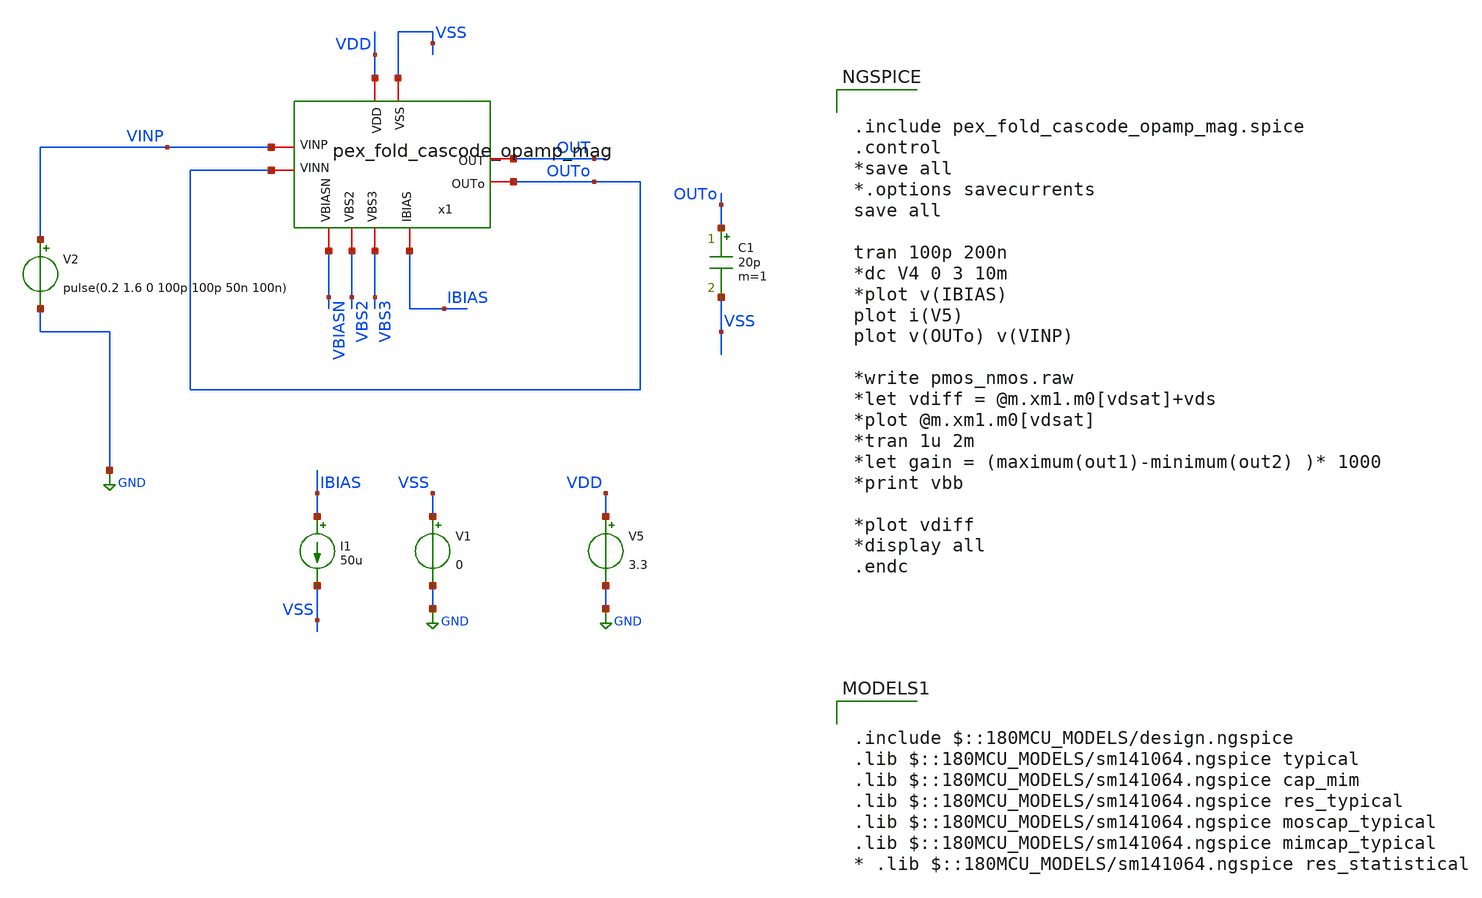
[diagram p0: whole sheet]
** sch_path: SCOP_INPUT_AND_MUX_PAKISTAN_03/Xschem/Folded_single/folded_single_TB_slew.sch
**.subckt folded_single_TB_slew
V5 VDD GND 3.3
V2 VINP GND pulse(0.2 1.6 0 100p 100p 50n 100n)
V1 VSS GND 0
I1 IBIAS VSS 50u
C1 OUTo VSS 20p m=1
x1 OUT VDD VSS OUTo VINP IBIAS VBS2 VBS3 VBIASN OUTo pex_fold_cascode_opamp_mag
**** begin user architecture code


.include pex_fold_cascode_opamp_mag.spice
.control
*save all
*.options savecurrents
save all

tran 100p 200n
*dc V4 0 3 10m
*plot v(IBIAS)
plot i(V5)
plot v(OUTo) v(VINP)

*write pmos_nmos.raw
*let vdiff = @m.xm1.m0[vdsat]+vds
*plot @m.xm1.m0[vdsat]
*tran 1u 2m
*let gain = (maximum(out1)-minimum(out2) )* 1000
*print vbb

*plot vdiff
*display all
.endc



.include $::180MCU_MODELS/design.ngspice
.lib $::180MCU_MODELS/sm141064.ngspice typical
.lib $::180MCU_MODELS/sm141064.ngspice cap_mim
.lib $::180MCU_MODELS/sm141064.ngspice res_typical
.lib $::180MCU_MODELS/sm141064.ngspice moscap_typical
.lib $::180MCU_MODELS/sm141064.ngspice mimcap_typical
* .lib $::180MCU_MODELS/sm141064.ngspice res_statistical

**** end user architecture code
**.ends
.GLOBAL GND
.end
